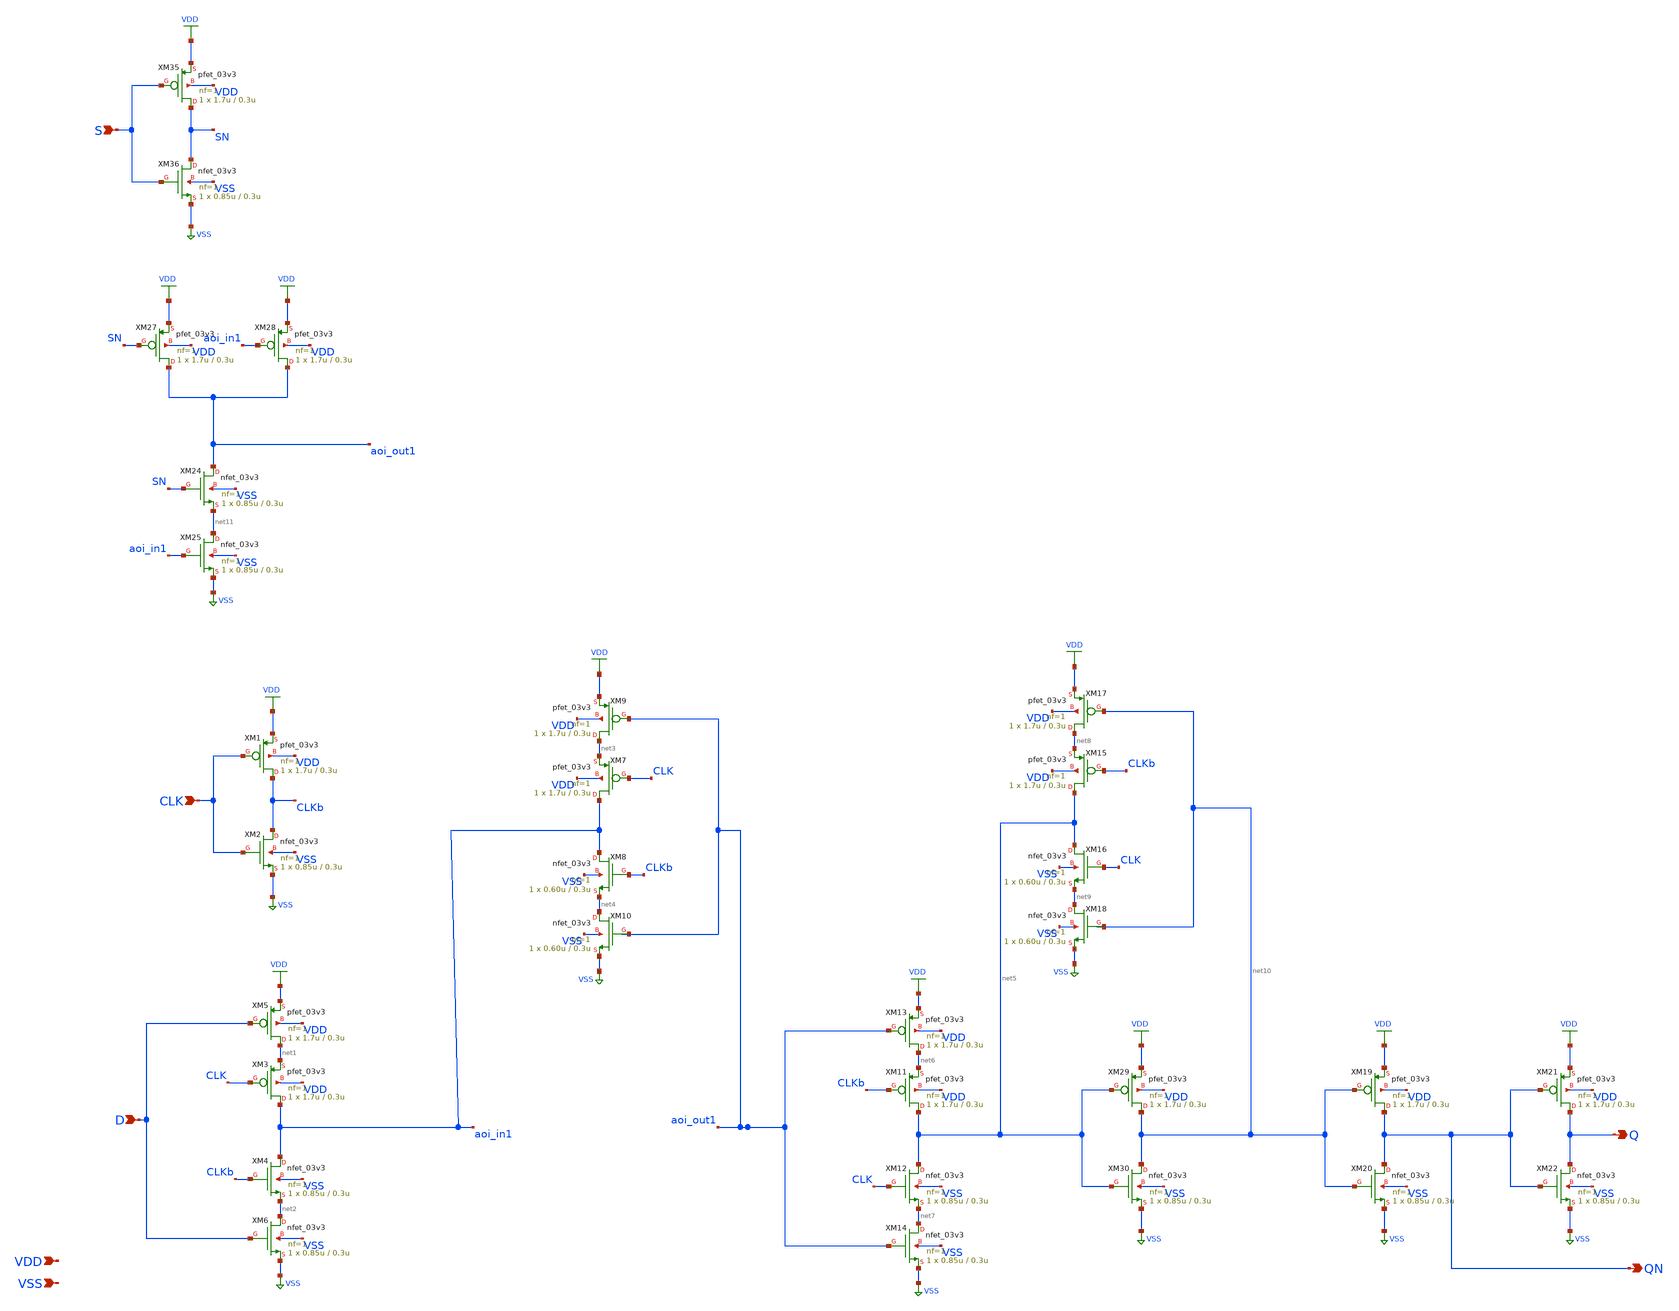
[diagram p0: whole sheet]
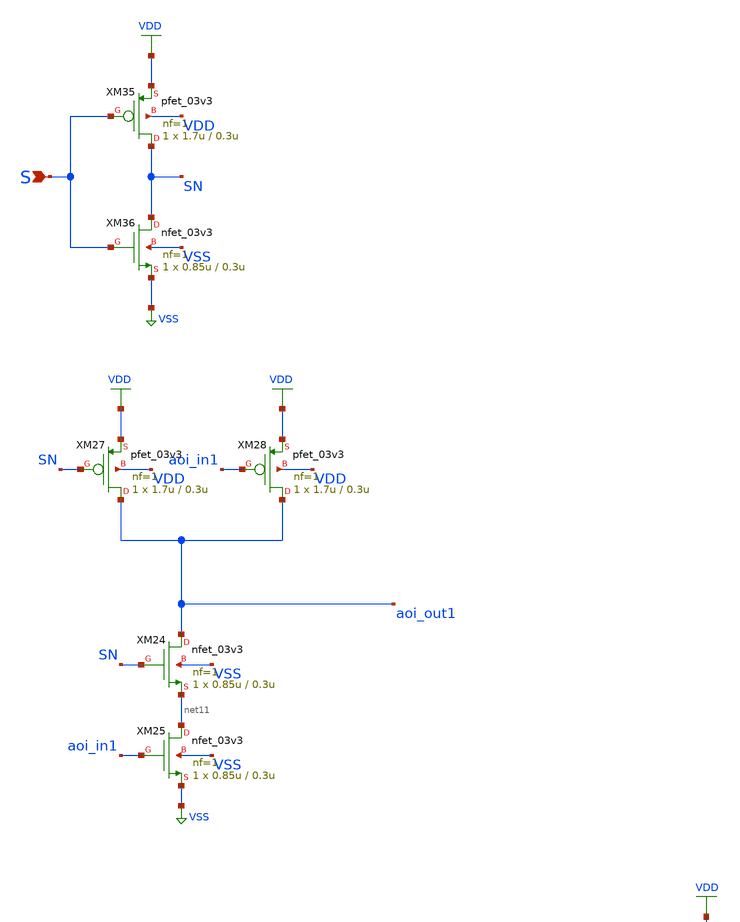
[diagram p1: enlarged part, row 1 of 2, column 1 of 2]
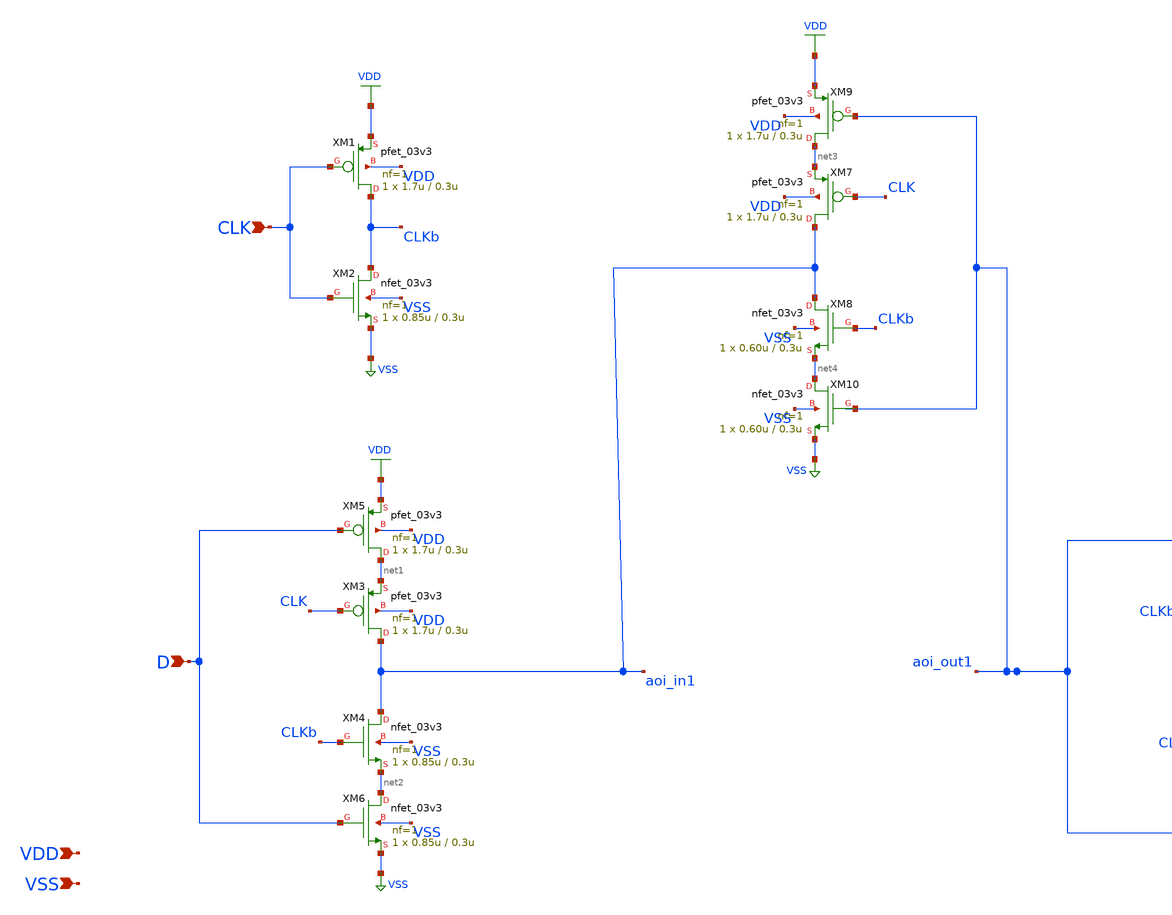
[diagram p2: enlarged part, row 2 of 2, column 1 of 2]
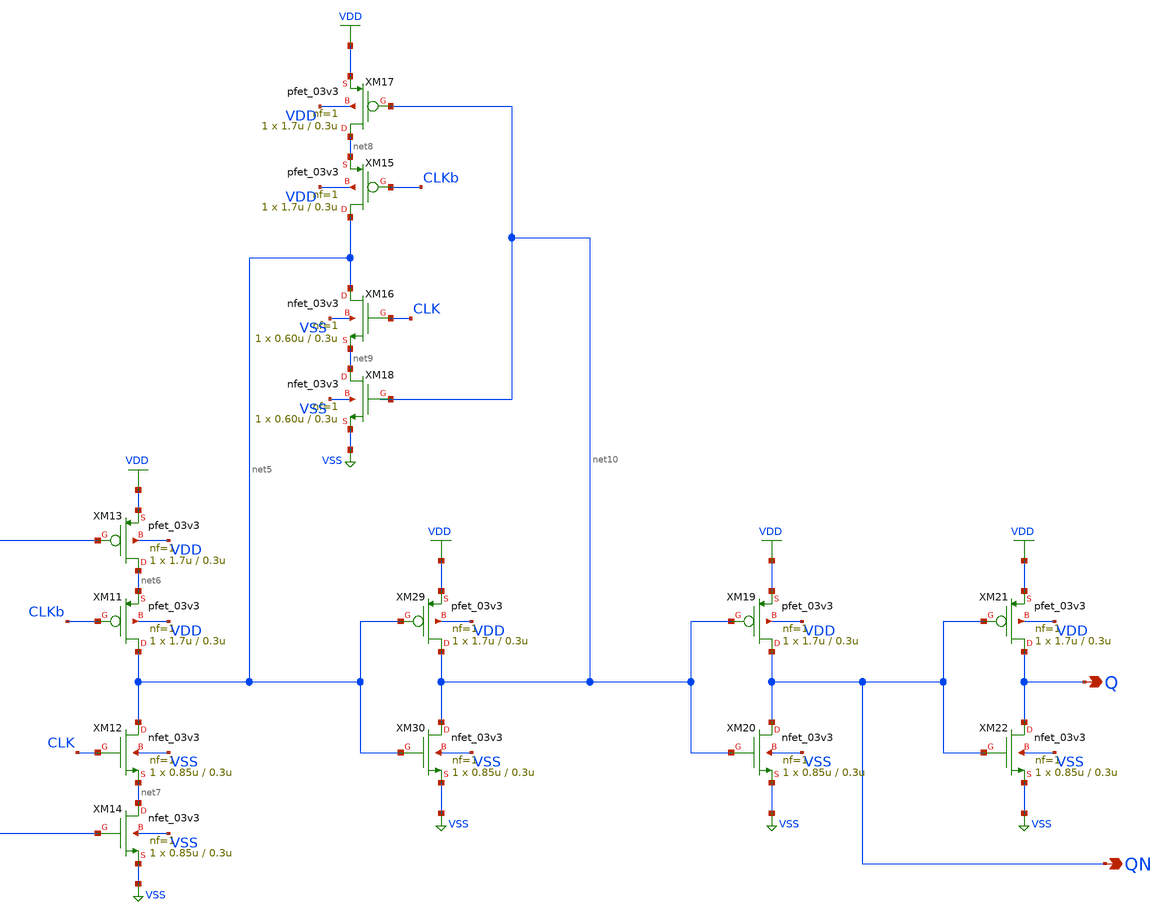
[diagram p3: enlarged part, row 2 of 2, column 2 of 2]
** sch_path: gf180mcu_osu_sc_gp12t3v3/xschem/gf180mcu_osu_sc_gp12t3v3__dffs_1.sch
**.subckt gf180mcu_osu_sc_gp12t3v3__dffs_1 D CLK Q QN S VDD VSS
*.ipin D
*.ipin CLK
*.opin Q
*.opin QN
*.ipin S
*.ipin VDD
*.ipin VSS
XM1 CLKb CLK VDD VDD pfet_03v3 L=0.3u W=1.7u nf=1 ad='int((nf+1)/2) * W/nf * 0.18u' as='int((nf+2)/2) * W/nf * 0.18u'
+ pd='2*int((nf+1)/2) * (W/nf + 0.18u)' ps='2*int((nf+2)/2) * (W/nf + 0.18u)' nrd='0.18u / W' nrs='0.18u / W'
+ sa=0 sb=0 sd=0 m=1
XM2 CLKb CLK VSS VSS nfet_03v3 L=0.3u W=0.85u nf=1 ad='int((nf+1)/2) * W/nf * 0.18u' as='int((nf+2)/2) * W/nf * 0.18u'
+ pd='2*int((nf+1)/2) * (W/nf + 0.18u)' ps='2*int((nf+2)/2) * (W/nf + 0.18u)' nrd='0.18u / W' nrs='0.18u / W'
+ sa=0 sb=0 sd=0 m=1
XM3 aoi_in1 CLK net1 VDD pfet_03v3 L=0.3u W=1.7u nf=1 ad='int((nf+1)/2) * W/nf * 0.18u' as='int((nf+2)/2) * W/nf * 0.18u'
+ pd='2*int((nf+1)/2) * (W/nf + 0.18u)' ps='2*int((nf+2)/2) * (W/nf + 0.18u)' nrd='0.18u / W' nrs='0.18u / W'
+ sa=0 sb=0 sd=0 m=1
XM4 aoi_in1 CLKb net2 VSS nfet_03v3 L=0.3u W=0.85u nf=1 ad='int((nf+1)/2) * W/nf * 0.18u' as='int((nf+2)/2) * W/nf * 0.18u'
+ pd='2*int((nf+1)/2) * (W/nf + 0.18u)' ps='2*int((nf+2)/2) * (W/nf + 0.18u)' nrd='0.18u / W' nrs='0.18u / W'
+ sa=0 sb=0 sd=0 m=1
XM5 net1 D VDD VDD pfet_03v3 L=0.3u W=1.7u nf=1 ad='int((nf+1)/2) * W/nf * 0.18u' as='int((nf+2)/2) * W/nf * 0.18u'
+ pd='2*int((nf+1)/2) * (W/nf + 0.18u)' ps='2*int((nf+2)/2) * (W/nf + 0.18u)' nrd='0.18u / W' nrs='0.18u / W'
+ sa=0 sb=0 sd=0 m=1
XM6 net2 D VSS VSS nfet_03v3 L=0.3u W=0.85u nf=1 ad='int((nf+1)/2) * W/nf * 0.18u' as='int((nf+2)/2) * W/nf * 0.18u'
+ pd='2*int((nf+1)/2) * (W/nf + 0.18u)' ps='2*int((nf+2)/2) * (W/nf + 0.18u)' nrd='0.18u / W' nrs='0.18u / W'
+ sa=0 sb=0 sd=0 m=1
XM7 aoi_in1 CLK net3 VDD pfet_03v3 L=0.3u W=1.7u nf=1 ad='int((nf+1)/2) * W/nf * 0.18u' as='int((nf+2)/2) * W/nf * 0.18u'
+ pd='2*int((nf+1)/2) * (W/nf + 0.18u)' ps='2*int((nf+2)/2) * (W/nf + 0.18u)' nrd='0.18u / W' nrs='0.18u / W'
+ sa=0 sb=0 sd=0 m=1
XM8 aoi_in1 CLKb net4 VSS nfet_03v3 L=0.3u W=0.60u nf=1 ad='int((nf+1)/2) * W/nf * 0.18u' as='int((nf+2)/2) * W/nf * 0.18u'
+ pd='2*int((nf+1)/2) * (W/nf + 0.18u)' ps='2*int((nf+2)/2) * (W/nf + 0.18u)' nrd='0.18u / W' nrs='0.18u / W'
+ sa=0 sb=0 sd=0 m=1
XM9 net3 aoi_out1 VDD VDD pfet_03v3 L=0.3u W=1.7u nf=1 ad='int((nf+1)/2) * W/nf * 0.18u' as='int((nf+2)/2) * W/nf * 0.18u'
+ pd='2*int((nf+1)/2) * (W/nf + 0.18u)' ps='2*int((nf+2)/2) * (W/nf + 0.18u)' nrd='0.18u / W' nrs='0.18u / W'
+ sa=0 sb=0 sd=0 m=1
XM10 net4 aoi_out1 VSS VSS nfet_03v3 L=0.3u W=0.60u nf=1 ad='int((nf+1)/2) * W/nf * 0.18u' as='int((nf+2)/2) * W/nf * 0.18u'
+ pd='2*int((nf+1)/2) * (W/nf + 0.18u)' ps='2*int((nf+2)/2) * (W/nf + 0.18u)' nrd='0.18u / W' nrs='0.18u / W'
+ sa=0 sb=0 sd=0 m=1
XM11 net5 CLKb net6 VDD pfet_03v3 L=0.3u W=1.7u nf=1 ad='int((nf+1)/2) * W/nf * 0.18u' as='int((nf+2)/2) * W/nf * 0.18u'
+ pd='2*int((nf+1)/2) * (W/nf + 0.18u)' ps='2*int((nf+2)/2) * (W/nf + 0.18u)' nrd='0.18u / W' nrs='0.18u / W'
+ sa=0 sb=0 sd=0 m=1
XM12 net5 CLK net7 VSS nfet_03v3 L=0.3u W=0.85u nf=1 ad='int((nf+1)/2) * W/nf * 0.18u' as='int((nf+2)/2) * W/nf * 0.18u'
+ pd='2*int((nf+1)/2) * (W/nf + 0.18u)' ps='2*int((nf+2)/2) * (W/nf + 0.18u)' nrd='0.18u / W' nrs='0.18u / W'
+ sa=0 sb=0 sd=0 m=1
XM13 net6 aoi_out1 VDD VDD pfet_03v3 L=0.3u W=1.7u nf=1 ad='int((nf+1)/2) * W/nf * 0.18u' as='int((nf+2)/2) * W/nf * 0.18u'
+ pd='2*int((nf+1)/2) * (W/nf + 0.18u)' ps='2*int((nf+2)/2) * (W/nf + 0.18u)' nrd='0.18u / W' nrs='0.18u / W'
+ sa=0 sb=0 sd=0 m=1
XM14 net7 aoi_out1 VSS VSS nfet_03v3 L=0.3u W=0.85u nf=1 ad='int((nf+1)/2) * W/nf * 0.18u' as='int((nf+2)/2) * W/nf * 0.18u'
+ pd='2*int((nf+1)/2) * (W/nf + 0.18u)' ps='2*int((nf+2)/2) * (W/nf + 0.18u)' nrd='0.18u / W' nrs='0.18u / W'
+ sa=0 sb=0 sd=0 m=1
XM15 net5 CLKb net8 VDD pfet_03v3 L=0.3u W=1.7u nf=1 ad='int((nf+1)/2) * W/nf * 0.18u' as='int((nf+2)/2) * W/nf * 0.18u'
+ pd='2*int((nf+1)/2) * (W/nf + 0.18u)' ps='2*int((nf+2)/2) * (W/nf + 0.18u)' nrd='0.18u / W' nrs='0.18u / W'
+ sa=0 sb=0 sd=0 m=1
XM16 net5 CLK net9 VSS nfet_03v3 L=0.3u W=0.60u nf=1 ad='int((nf+1)/2) * W/nf * 0.18u' as='int((nf+2)/2) * W/nf * 0.18u'
+ pd='2*int((nf+1)/2) * (W/nf + 0.18u)' ps='2*int((nf+2)/2) * (W/nf + 0.18u)' nrd='0.18u / W' nrs='0.18u / W'
+ sa=0 sb=0 sd=0 m=1
XM17 net8 net10 VDD VDD pfet_03v3 L=0.3u W=1.7u nf=1 ad='int((nf+1)/2) * W/nf * 0.18u' as='int((nf+2)/2) * W/nf * 0.18u'
+ pd='2*int((nf+1)/2) * (W/nf + 0.18u)' ps='2*int((nf+2)/2) * (W/nf + 0.18u)' nrd='0.18u / W' nrs='0.18u / W'
+ sa=0 sb=0 sd=0 m=1
XM18 net9 net10 VSS VSS nfet_03v3 L=0.3u W=0.60u nf=1 ad='int((nf+1)/2) * W/nf * 0.18u' as='int((nf+2)/2) * W/nf * 0.18u'
+ pd='2*int((nf+1)/2) * (W/nf + 0.18u)' ps='2*int((nf+2)/2) * (W/nf + 0.18u)' nrd='0.18u / W' nrs='0.18u / W'
+ sa=0 sb=0 sd=0 m=1
XM19 QN net10 VDD VDD pfet_03v3 L=0.3u W=1.7u nf=1 ad='int((nf+1)/2) * W/nf * 0.18u' as='int((nf+2)/2) * W/nf * 0.18u'
+ pd='2*int((nf+1)/2) * (W/nf + 0.18u)' ps='2*int((nf+2)/2) * (W/nf + 0.18u)' nrd='0.18u / W' nrs='0.18u / W'
+ sa=0 sb=0 sd=0 m=1
XM20 QN net10 VSS VSS nfet_03v3 L=0.3u W=0.85u nf=1 ad='int((nf+1)/2) * W/nf * 0.18u' as='int((nf+2)/2) * W/nf * 0.18u'
+ pd='2*int((nf+1)/2) * (W/nf + 0.18u)' ps='2*int((nf+2)/2) * (W/nf + 0.18u)' nrd='0.18u / W' nrs='0.18u / W'
+ sa=0 sb=0 sd=0 m=1
XM21 Q QN VDD VDD pfet_03v3 L=0.3u W=1.7u nf=1 ad='int((nf+1)/2) * W/nf * 0.18u' as='int((nf+2)/2) * W/nf * 0.18u'
+ pd='2*int((nf+1)/2) * (W/nf + 0.18u)' ps='2*int((nf+2)/2) * (W/nf + 0.18u)' nrd='0.18u / W' nrs='0.18u / W'
+ sa=0 sb=0 sd=0 m=1
XM22 Q QN VSS VSS nfet_03v3 L=0.3u W=0.85u nf=1 ad='int((nf+1)/2) * W/nf * 0.18u' as='int((nf+2)/2) * W/nf * 0.18u'
+ pd='2*int((nf+1)/2) * (W/nf + 0.18u)' ps='2*int((nf+2)/2) * (W/nf + 0.18u)' nrd='0.18u / W' nrs='0.18u / W'
+ sa=0 sb=0 sd=0 m=1
XM24 aoi_out1 SN net11 VSS nfet_03v3 L=0.3u W=0.85u nf=1 ad='int((nf+1)/2) * W/nf * 0.18u' as='int((nf+2)/2) * W/nf * 0.18u'
+ pd='2*int((nf+1)/2) * (W/nf + 0.18u)' ps='2*int((nf+2)/2) * (W/nf + 0.18u)' nrd='0.18u / W' nrs='0.18u / W'
+ sa=0 sb=0 sd=0 m=1
XM25 net11 aoi_in1 VSS VSS nfet_03v3 L=0.3u W=0.85u nf=1 ad='int((nf+1)/2) * W/nf * 0.18u' as='int((nf+2)/2) * W/nf * 0.18u'
+ pd='2*int((nf+1)/2) * (W/nf + 0.18u)' ps='2*int((nf+2)/2) * (W/nf + 0.18u)' nrd='0.18u / W' nrs='0.18u / W'
+ sa=0 sb=0 sd=0 m=1
XM27 aoi_out1 SN VDD VDD pfet_03v3 L=0.3u W=1.7u nf=1 ad='int((nf+1)/2) * W/nf * 0.18u' as='int((nf+2)/2) * W/nf * 0.18u'
+ pd='2*int((nf+1)/2) * (W/nf + 0.18u)' ps='2*int((nf+2)/2) * (W/nf + 0.18u)' nrd='0.18u / W' nrs='0.18u / W'
+ sa=0 sb=0 sd=0 m=1
XM28 aoi_out1 aoi_in1 VDD VDD pfet_03v3 L=0.3u W=1.7u nf=1 ad='int((nf+1)/2) * W/nf * 0.18u' as='int((nf+2)/2) * W/nf * 0.18u'
+ pd='2*int((nf+1)/2) * (W/nf + 0.18u)' ps='2*int((nf+2)/2) * (W/nf + 0.18u)' nrd='0.18u / W' nrs='0.18u / W'
+ sa=0 sb=0 sd=0 m=1
XM35 SN S VDD VDD pfet_03v3 L=0.3u W=1.7u nf=1 ad='int((nf+1)/2) * W/nf * 0.18u' as='int((nf+2)/2) * W/nf * 0.18u'
+ pd='2*int((nf+1)/2) * (W/nf + 0.18u)' ps='2*int((nf+2)/2) * (W/nf + 0.18u)' nrd='0.18u / W' nrs='0.18u / W'
+ sa=0 sb=0 sd=0 m=1
XM36 SN S VSS VSS nfet_03v3 L=0.3u W=0.85u nf=1 ad='int((nf+1)/2) * W/nf * 0.18u' as='int((nf+2)/2) * W/nf * 0.18u'
+ pd='2*int((nf+1)/2) * (W/nf + 0.18u)' ps='2*int((nf+2)/2) * (W/nf + 0.18u)' nrd='0.18u / W' nrs='0.18u / W'
+ sa=0 sb=0 sd=0 m=1
XM29 net10 net5 VDD VDD pfet_03v3 L=0.3u W=1.7u nf=1 ad='int((nf+1)/2) * W/nf * 0.18u' as='int((nf+2)/2) * W/nf * 0.18u'
+ pd='2*int((nf+1)/2) * (W/nf + 0.18u)' ps='2*int((nf+2)/2) * (W/nf + 0.18u)' nrd='0.18u / W' nrs='0.18u / W'
+ sa=0 sb=0 sd=0 m=1
XM30 net10 net5 VSS VSS nfet_03v3 L=0.3u W=0.85u nf=1 ad='int((nf+1)/2) * W/nf * 0.18u' as='int((nf+2)/2) * W/nf * 0.18u'
+ pd='2*int((nf+1)/2) * (W/nf + 0.18u)' ps='2*int((nf+2)/2) * (W/nf + 0.18u)' nrd='0.18u / W' nrs='0.18u / W'
+ sa=0 sb=0 sd=0 m=1
**.ends
.GLOBAL VDD
.GLOBAL VSS
.end
